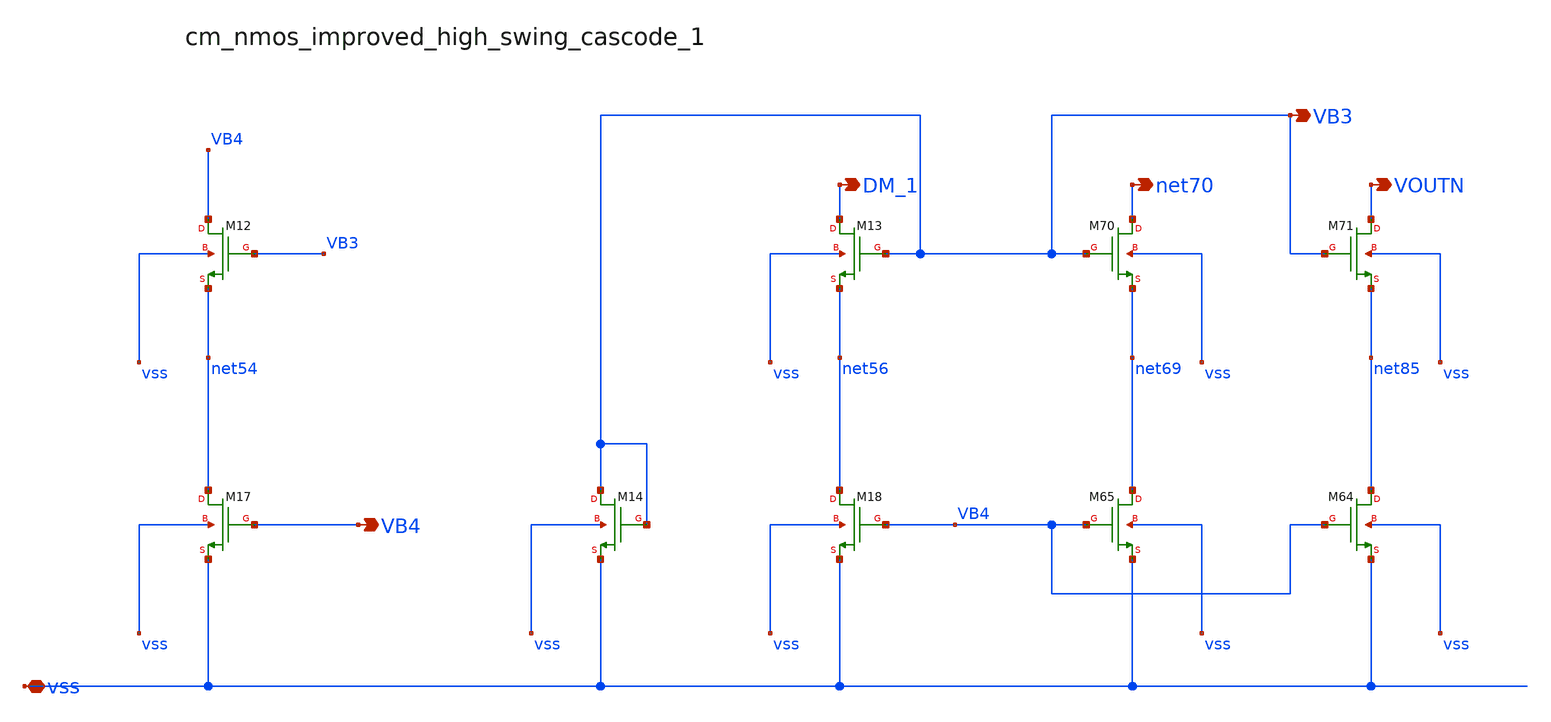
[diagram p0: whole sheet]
** sch_path: analog-db/raw/amp_016_song_dacfc/hier/blocks/cm_nmos_improved_high_swing_cascode_1.sch
**.subckt cm_nmos_improved_high_swing_cascode_1 vss VB4 DM_1 net70 VOUTN VB3
*.iopin vss
*.opin VB4
*.opin DM_1
*.opin net70
*.opin VOUTN
*.opin VB3
XM12 VB4 VB3 net54 vss sg13_lv_nmos w=x_dut_xm12_w l=x_dut_xm12_l ng=1 m=x_dut_xm12_m
XM13 DM_1 VB3 net56 vss sg13_lv_nmos w=x_dut_xm13_w l=x_dut_xm13_l ng=1 m=x_dut_xm13_m
XM14 VB3 VB3 vss vss sg13_lv_nmos w=x_dut_xm14_w l=x_dut_xm14_l ng=1 m=x_dut_xm14_m
XM17 net54 VB4 vss vss sg13_lv_nmos w=x_dut_xm17_w l=x_dut_xm17_l ng=1 m=x_dut_xm17_m
XM18 net56 VB4 vss vss sg13_lv_nmos w=x_dut_xm18_w l=x_dut_xm18_l ng=1 m=x_dut_xm18_m
XM64 net85 VB4 vss vss sg13_lv_nmos w=x_dut_xm64_w l=x_dut_xm64_l ng=1 m=x_dut_xm64_m
XM65 net69 VB4 vss vss sg13_lv_nmos w=x_dut_xm65_w l=x_dut_xm65_l ng=1 m=x_dut_xm65_m
XM70 net70 VB3 net69 vss sg13_lv_nmos w=x_dut_xm70_w l=x_dut_xm70_l ng=1 m=x_dut_xm70_m
XM71 VOUTN VB3 net85 vss sg13_lv_nmos w=x_dut_xm71_w l=x_dut_xm71_l ng=1 m=x_dut_xm71_m
**.ends
.end
